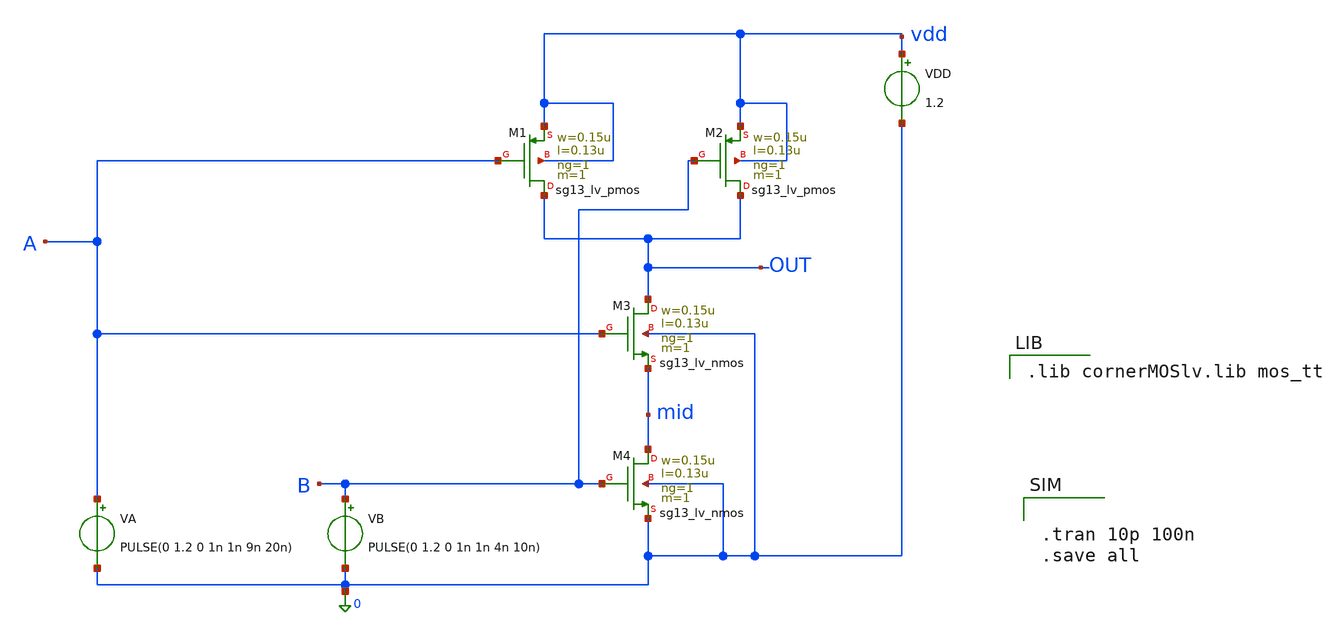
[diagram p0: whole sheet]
** sch_path: Test_InverterWave.sch
**.subckt Test_InverterWave
XM1 OUT A vdd vdd sg13_lv_pmos w=0.15u l=0.13u ng=1 m=1 mm_ok=1
XM2 OUT B vdd vdd sg13_lv_pmos w=0.15u l=0.13u ng=1 m=1 mm_ok=1
XM3 OUT A mid 0 sg13_lv_nmos w=0.15u l=0.13u ng=1 m=1 mm_ok=1
XM4 mid B 0 0 sg13_lv_nmos w=0.15u l=0.13u ng=1 m=1 mm_ok=1
VB B 0 PULSE(0 1.2 0 1n 1n 4n 10n)
VA A 0 PULSE(0 1.2 0 1n 1n 9n 20n)
VDD vdd 0 1.2
**** begin user architecture code

.lib cornerMOSlv.lib mos_tt



.tran 10p 100n
.save all


**** end user architecture code
**.ends
.end
